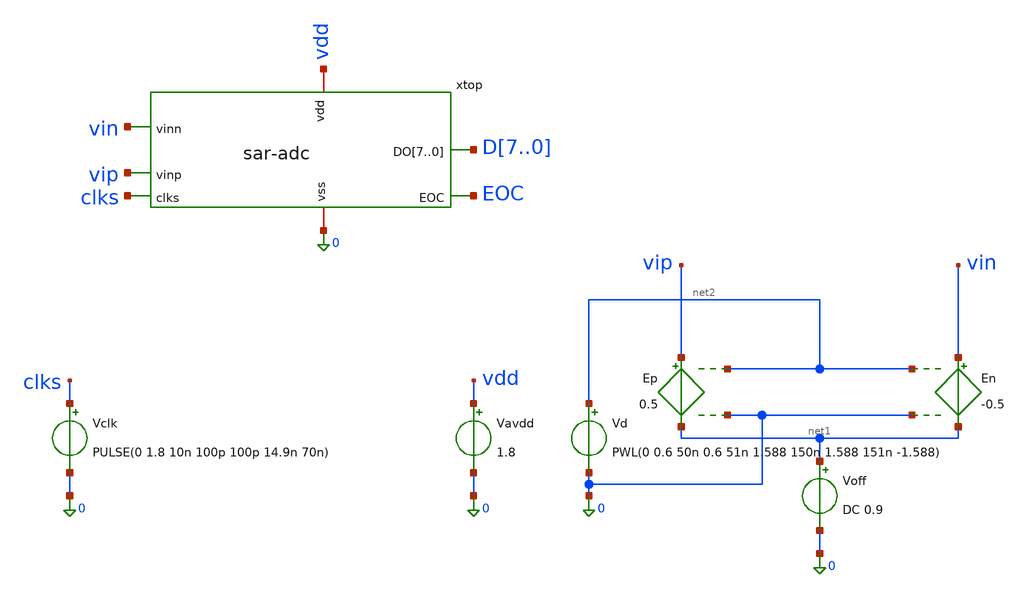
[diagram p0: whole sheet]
** sch_path: xschem/sar-adc_tb/sar-adc_tb.sch
.lib $::SKYWATER_MODELS/sky130.lib.spice tt
.include $::SKYWATER_STDCELLS/sky130_fd_sc_hd.spice

**.subckt sar-adc_tb
xtop vin vip clks D7 D6 D5 D4 D3 D2 D1 D0 vdd 0 EOC sar-adc
Vclk clks 0 PULSE(0 1.8 10n 100p 100p 14.9n 70n)
.save i(vclk)
Vavdd vdd 0 1.8
.save i(vavdd)
Voff net1 0 DC 0.9
.save i(voff)
En vin net1 net2 0 -0.5
Ep vip net1 net2 0 0.5
Vd net2 0 PWL(0 0.6 50n 0.6 51n 1.588 150n 1.588 151n -1.588)
.save i(vd)
**** begin user architecture code



.control
 remzerovec
 save v(clks) v(EOC) v(vip) v(vin) v(xtop.d7) v(xtop.d6) v(xtop.d5) v(xtop.d4) v(xtop.d3) v(xtop.d2)
+ v(xtop.d1) v(xtop.d0) v(xtop.ctopp) v(xtop.ctopn) v(xtop.clkc) v(xtop.comp_valid) v(xtop.comp_vop)
+ v(xtop.comp_von) v(xtop.clk1) v(xtop.clk2) v(xtop.clk3) v(xtop.clk4) v(xtop.clk5) v(xtop.clk6) v(xtop.clk7)
+ v(xtop.clk8) v(xtop.xcomparator.vtail)
 + v(xtop.xcomparator.pcp) v(xtop.xcomparator.pcn)
 + v(d7) v(d6) v(d5) v(d4) v(d3) v(d2) v(d1) v(d0)
 tran 20p 350n
 write sar-adc_tb.raw
.endc





.param nfft = 64
.param mcyc = 29
.param fs = 10e6
.param fin  = 'mcyc/nfft*fs'     $ 4.53125 MHz
.param amp  = 0.88               $ hampir full-scale single-ended
.param off  = 0.9                $ V_CM
.param namp = '-amp'             $ amplitudo sisi n (fase berlawanan)
.options reltol=1e-4 vntol=1e-8 abstol=1e-14 chgtol=1e-16


**** end user architecture code
**.ends
.end
